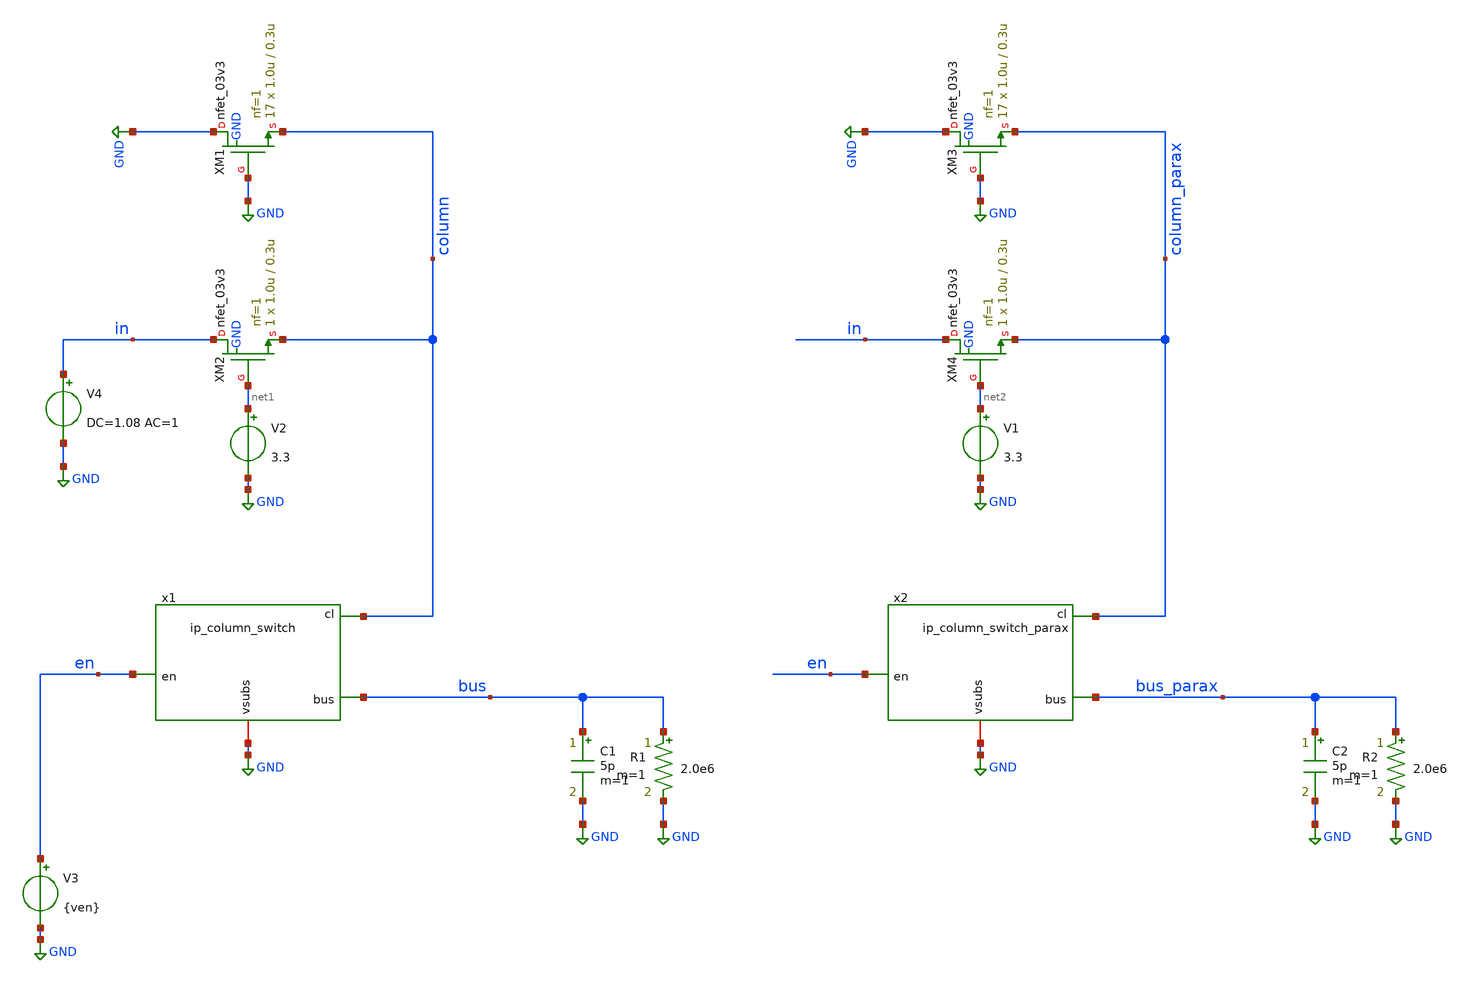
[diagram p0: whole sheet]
** sch_path: xschem/tb_column_switch_ac.sch
**.subckt tb_column_switch_ac
x1 column bus en GND ip_column_switch
XM1 GND GND column GND nfet_03v3 L=0.3u W=1.0u nf=1 ad='int((nf+1)/2) * W/nf * 0.18u' as='int((nf+2)/2) * W/nf * 0.18u'
+ pd='2*int((nf+1)/2) * (W/nf + 0.18u)' ps='2*int((nf+2)/2) * (W/nf + 0.18u)' nrd='0.18u / W' nrs='0.18u / W'
+ sa=0 sb=0 sd=0 m=17 par=17
XM2 in net1 column GND nfet_03v3 L=0.3u W=1.0u nf=1 ad='int((nf+1)/2) * W/nf * 0.18u' as='int((nf+2)/2) * W/nf * 0.18u'
+ pd='2*int((nf+1)/2) * (W/nf + 0.18u)' ps='2*int((nf+2)/2) * (W/nf + 0.18u)' nrd='0.18u / W' nrs='0.18u / W'
+ sa=0 sb=0 sd=0 m=1 par=1
V2 net1 GND 3.3
V3 en GND {ven}
V4 in GND DC=1.08 AC=1
R1 bus GND 2.0e6 m=1
C1 bus GND 5p m=1
x2 column_parax bus_parax en GND ip_column_switch_parax
XM3 GND GND column_parax GND nfet_03v3 L=0.3u W=1.0u nf=1 ad='int((nf+1)/2) * W/nf * 0.18u' as='int((nf+2)/2) * W/nf * 0.18u'
+ pd='2*int((nf+1)/2) * (W/nf + 0.18u)' ps='2*int((nf+2)/2) * (W/nf + 0.18u)' nrd='0.18u / W' nrs='0.18u / W'
+ sa=0 sb=0 sd=0 m=17 par=17
XM4 in net2 column_parax GND nfet_03v3 L=0.3u W=1.0u nf=1 ad='int((nf+1)/2) * W/nf * 0.18u' as='int((nf+2)/2) * W/nf * 0.18u'
+ pd='2*int((nf+1)/2) * (W/nf + 0.18u)' ps='2*int((nf+2)/2) * (W/nf + 0.18u)' nrd='0.18u / W' nrs='0.18u / W'
+ sa=0 sb=0 sd=0 m=1 par=1
V1 net2 GND 3.3
R2 bus_parax GND 2.0e6 m=1
C2 bus_parax GND 5p m=1
**** begin user architecture code

.lib $::180MCU_MODELS/sm141064.ngspice statistical
.lib $::180MCU_MODELS/sm141064.ngspice moscap_typical
.lib $::180MCU_MODELS/sm141064.ngspice diode_typical
.lib $::180MCU_MODELS/sm141064.ngspice res_statistical




# Global parameters typically sourced from design.ngspice
.param sw_stat_global   = 1
.param sw_stat_mismatch = 1
.param mc_skew          = 1
.param res_mc_skew=3
.param cap_mc_skew=3
.param fnoicor=0

.param ven = 3.3

.control
	save all
	foreach venv 0.0 3.3
		repeat 10
			mc_source
			alterparam ven = $venv
			reset
			ac dec 1000 1 100Meg
			write tb_column_switch_ac.raw
			set appendwrite
			reset
		end
	end
	quit
.endc



**** end user architecture code
**.ends

* expanding   symbol:  ip_column_switch.sym # of pins=4
** sym_path: xschem/ip_column_switch.sym
** sch_path: xschem/ip_column_switch.sch
.subckt ip_column_switch cl bus en vsubs
*.ipin cl
*.ipin en
*.iopin vsubs
*.opin bus
XM1 cl en bus vsubs nfet_06v0 L=0.7u W=0.5u nf=1 ad='int((nf+1)/2) * W/nf * 0.18u' as='int((nf+2)/2) * W/nf * 0.18u'
+ pd='2*int((nf+1)/2) * (W/nf + 0.18u)' ps='2*int((nf+2)/2) * (W/nf + 0.18u)' nrd='0.18u / W' nrs='0.18u / W'
+ sa=0 sb=0 sd=0 m=2 par=2
D1 vsubs en diode_nd2ps_06v0 area='0.5u * 0.5u ' pj='2*0.5u + 2*0.5u ' m=1
.ends


* expanding   symbol:  ip_column_switch_parax.sym # of pins=4
** sym_path: xschem/ip_column_switch.sym
.include [file normalize ./parax/ip_column_switch.sim.spice]
.GLOBAL GND
.end
